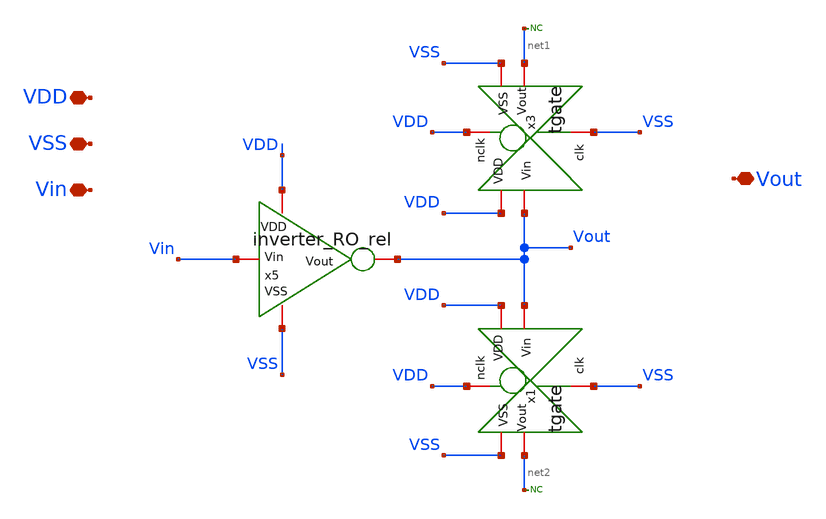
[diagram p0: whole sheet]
** sch_path: unic_cass_wrapper_user_project/ROs_reliability/rovcel2.sch
**.subckt rovcel2 VDD VSS Vin Vout
*.iopin VDD
*.iopin VSS
*.iopin Vin
*.iopin Vout
* noconn #net1
* noconn #net2
x5 VDD Vin Vout VSS inverter_RO_rel
x1 VDD VDD Vout net2 VSS VSS tgate
x3 VDD VDD Vout net1 VSS VSS tgate
**.ends

* expanding   symbol:  inverter_RO_rel.sym # of pins=4
** sym_path: inverter_RO_rel.sym
** sch_path: inverter_RO_rel.sch
.subckt inverter_RO_rel VDD Vin Vout VSS
*.iopin VDD
*.iopin VSS
*.iopin Vin
*.iopin Vout
XM3 Vout Vin VDD VDD sg13_lv_pmos w=3.4u l=0.45u ng=1 m=4 mm_ok=1
XM1 VSS Vin Vout VSS sg13_lv_nmos w=1.3u l=0.45u ng=1 m=4 mm_ok=1
.ends


* expanding   symbol:  tgate.sym # of pins=6
** sym_path: tgate.sym
** sch_path: tgate.sch
.subckt tgate nclk VDD Vin Vout VSS clk
*.iopin nclk
*.iopin clk
*.iopin VDD
*.iopin VSS
*.iopin Vout
*.iopin Vin
XM3 Vout nclk Vin VDD sg13_lv_pmos w=3.4u l=0.45u ng=1 m=1 mm_ok=1
XM1 Vout clk Vin VSS sg13_lv_nmos w=1.3u l=0.45u ng=1 m=1 mm_ok=1
.ends

.end
